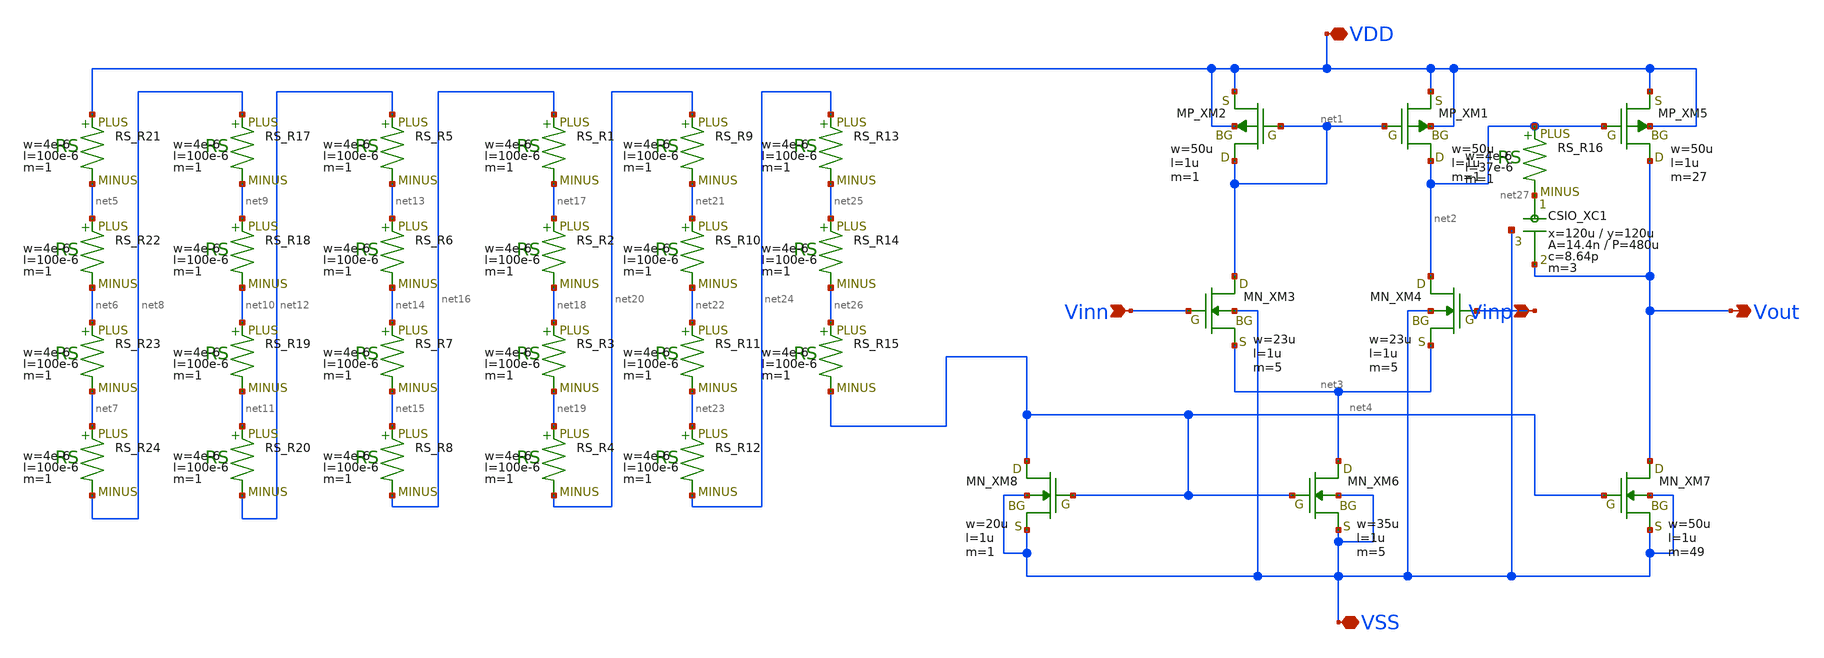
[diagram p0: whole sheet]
** sch_path: OPAF2026/OPAF001.sch
**.subckt OPAF001 Vout VDD VSS Vinn Vinp
*.opin Vout
*.iopin VDD
*.iopin VSS
*.ipin Vinn
*.ipin Vinp
XXM1 net2 net1 VDD VDD PMOS w=50u l=1u nrd=0 nrs=0 m=1
XXM2 net1 net1 VDD VDD PMOS w=50u l=1u nrd=0 nrs=0 m=1
XXM3 net1 Vinn net3 VSS NMOS w=23u l=1u nrd=0 nrs=0 m=5
XXM4 net2 Vinp net3 VSS NMOS w=23u l=1u nrd=0 nrs=0 m=5
XXM5 Vout net2 VDD VDD PMOS w=50u l=1u nrd=0 nrs=0 m=27
XXM6 net3 net4 VSS VSS NMOS w=35u l=1u nrd=0 nrs=0 m=5
XXM7 Vout net4 VSS VSS NMOS w=50u l=1u nrd=0 nrs=0 m=49
XXM8 net4 net4 VSS VSS NMOS w=20u l=1u nrd=0 nrs=0 m=1
XXC1 net27 Vout VSS F_CSIO c=8.64p x=120u y=120u m=3
XR1 net16 net17 F_RS w=4e-6 l=100e-6 R=1 tc1=0 tc2=0 m=1
XR2 net17 net18 F_RS w=4e-6 l=100e-6 R=1 tc1=0 tc2=0 m=1
XR3 net18 net19 F_RS w=4e-6 l=100e-6 R=1 tc1=0 tc2=0 m=1
XR4 net19 net20 F_RS w=4e-6 l=100e-6 R=1 tc1=0 tc2=0 m=1
XR5 net12 net13 F_RS w=4e-6 l=100e-6 R=1 tc1=0 tc2=0 m=1
XR6 net13 net14 F_RS w=4e-6 l=100e-6 R=1 tc1=0 tc2=0 m=1
XR7 net14 net15 F_RS w=4e-6 l=100e-6 R=1 tc1=0 tc2=0 m=1
XR8 net15 net16 F_RS w=4e-6 l=100e-6 R=1 tc1=0 tc2=0 m=1
XR9 net20 net21 F_RS w=4e-6 l=100e-6 R=1 tc1=0 tc2=0 m=1
XR10 net21 net22 F_RS w=4e-6 l=100e-6 R=1 tc1=0 tc2=0 m=1
XR11 net22 net23 F_RS w=4e-6 l=100e-6 R=1 tc1=0 tc2=0 m=1
XR12 net23 net24 F_RS w=4e-6 l=100e-6 R=1 tc1=0 tc2=0 m=1
XR13 net24 net25 F_RS w=4e-6 l=100e-6 R=1 tc1=0 tc2=0 m=1
XR14 net25 net26 F_RS w=4e-6 l=100e-6 R=1 tc1=0 tc2=0 m=1
XR15 net26 net4 F_RS w=4e-6 l=100e-6 R=1 tc1=0 tc2=0 m=1
XR17 net8 net9 F_RS w=4e-6 l=100e-6 R=1 tc1=0 tc2=0 m=1
XR18 net9 net10 F_RS w=4e-6 l=100e-6 R=1 tc1=0 tc2=0 m=1
XR19 net10 net11 F_RS w=4e-6 l=100e-6 R=1 tc1=0 tc2=0 m=1
XR20 net11 net12 F_RS w=4e-6 l=100e-6 R=1 tc1=0 tc2=0 m=1
XR21 VDD net5 F_RS w=4e-6 l=100e-6 R=1 tc1=0 tc2=0 m=1
XR22 net5 net6 F_RS w=4e-6 l=100e-6 R=1 tc1=0 tc2=0 m=1
XR23 net6 net7 F_RS w=4e-6 l=100e-6 R=1 tc1=0 tc2=0 m=1
XR24 net7 net8 F_RS w=4e-6 l=100e-6 R=1 tc1=0 tc2=0 m=1
XR16 net2 net27 F_RS w=4e-6 l=37e-6 R=1 tc1=0 tc2=0 m=1
**.ends
.end
